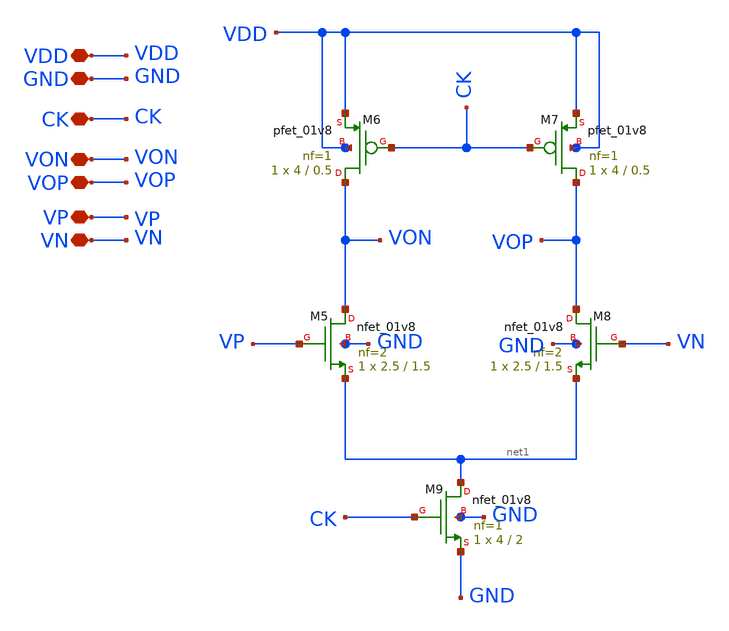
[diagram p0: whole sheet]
** sch_path: xschem/comparator/preamp.sch
**.subckt preamp VDD GND CK VON VOP VP VN
*.iopin VDD
*.iopin GND
*.iopin CK
*.iopin VON
*.iopin VOP
*.iopin VP
*.iopin VN
XM5 VON VP net1 GND sky130_fd_pr__nfet_01v8 L=1.5 W=2.5 nf=2 ad='int((2 + 1)/2) * 2.5 / 2 * 0.29' as='int((2 + 2)/2) * 2.5 / 2 * 0.29'
+ pd='2*int((2 + 1)/2) * (2.5 / 2 + 0.29)' ps='2*int((2 + 2)/2) * (2.5 / 2 + 0.29)' nrd='0.29 / 2.5 ' nrs='0.29 / 2.5 '
+ sa=0 sb=0 sd=0 mult=1 m=1
XM6 VON CK VDD VDD sky130_fd_pr__pfet_01v8 L=0.5 W=4 nf=1 ad='int((nf+1)/2) * W/nf * 0.29' as='int((nf+2)/2) * W/nf * 0.29'
+ pd='2*int((nf+1)/2) * (W/nf + 0.29)' ps='2*int((nf+2)/2) * (W/nf + 0.29)' nrd='0.29 / W' nrs='0.29 / W'
+ sa=0 sb=0 sd=0 mult=1 m=1
XM7 VOP CK VDD VDD sky130_fd_pr__pfet_01v8 L=0.5 W=4 nf=1 ad='int((nf+1)/2) * W/nf * 0.29' as='int((nf+2)/2) * W/nf * 0.29'
+ pd='2*int((nf+1)/2) * (W/nf + 0.29)' ps='2*int((nf+2)/2) * (W/nf + 0.29)' nrd='0.29 / W' nrs='0.29 / W'
+ sa=0 sb=0 sd=0 mult=1 m=1
XM8 VOP VN net1 GND sky130_fd_pr__nfet_01v8 L=1.5 W=2.5 nf=2 ad='int((2 + 1)/2) * 2.5 / 2 * 0.29' as='int((2 + 2)/2) * 2.5 / 2 * 0.29'
+ pd='2*int((2 + 1)/2) * (2.5 / 2 + 0.29)' ps='2*int((2 + 2)/2) * (2.5 / 2 + 0.29)' nrd='0.29 / 2.5 ' nrs='0.29 / 2.5 '
+ sa=0 sb=0 sd=0 mult=1 m=1
XM9 net1 CK GND GND sky130_fd_pr__nfet_01v8 L=2 W=4 nf=1 ad='int((1 + 1)/2) * 4 / 1 * 0.29' as='int((1 + 2)/2) * 4 / 1 * 0.29'
+ pd='2*int((1 + 1)/2) * (4 / 1 + 0.29)' ps='2*int((1 + 2)/2) * (4 / 1 + 0.29)' nrd='0.29 / 4 ' nrs='0.29 / 4 '
+ sa=0 sb=0 sd=0 mult=1 m=1
**.ends
.end
